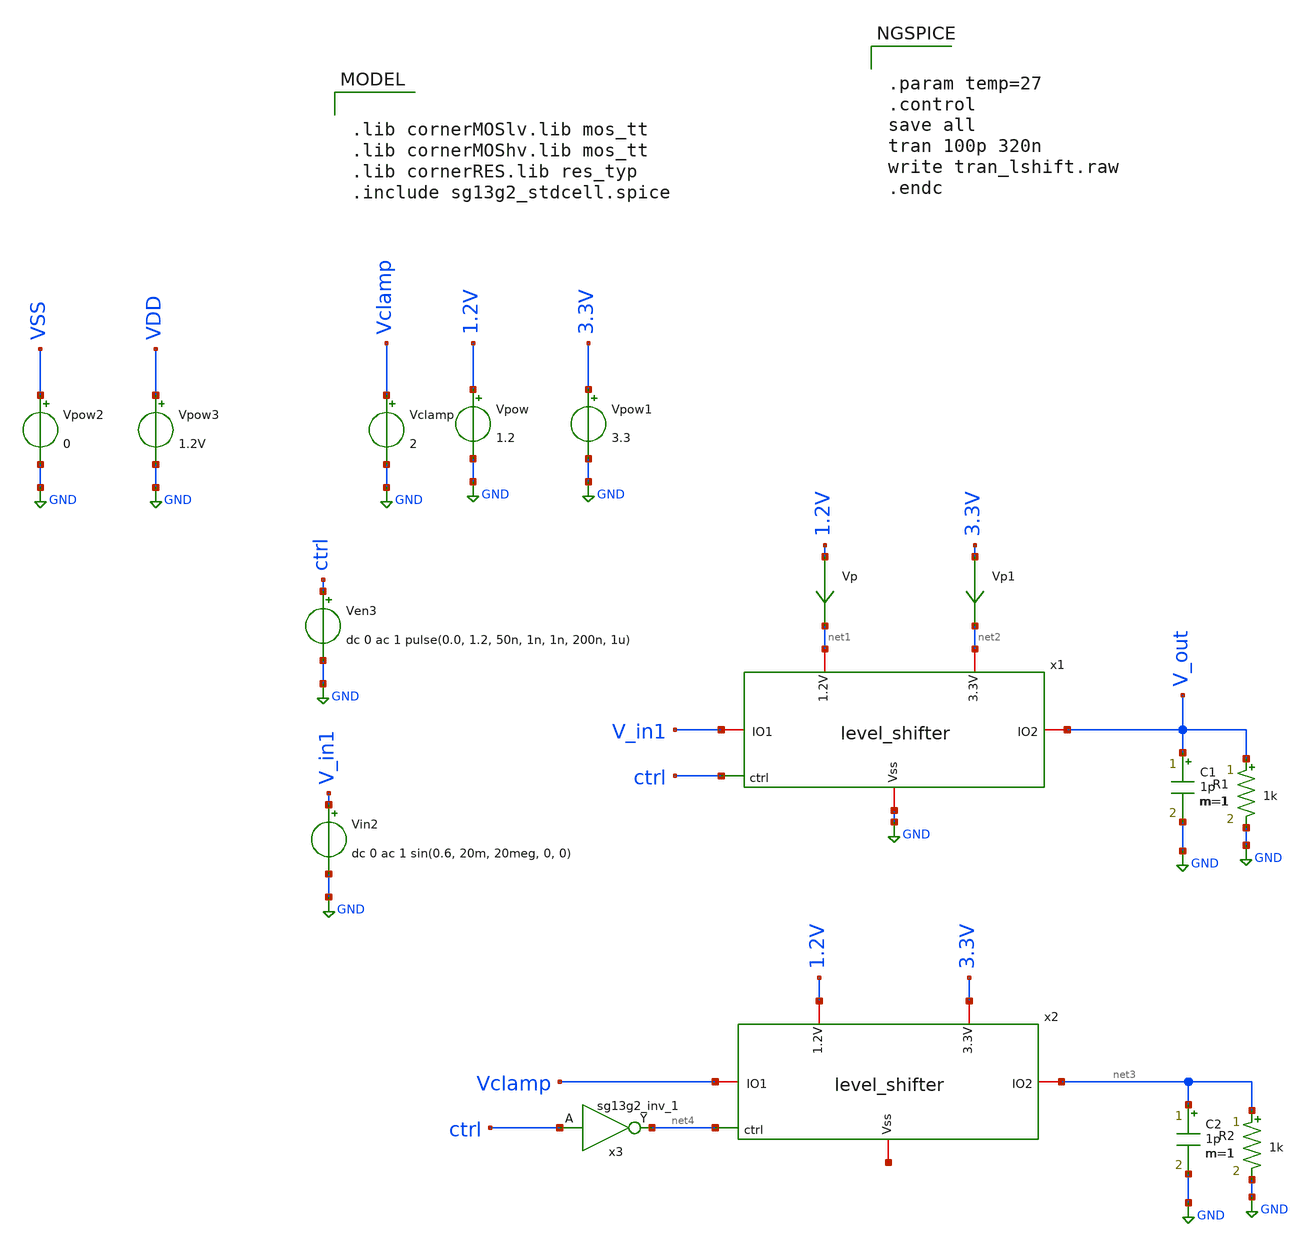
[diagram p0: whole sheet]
** sch_path: design_data/xschem/level_shifters_tb.sch
* Copyright 2023 IHP PDK Authors
* design_data/xschem/level_shifter.sch:
* Copyright 2025 IHP PDK Authors
**.subckt level_shifters_tb
Vpow 1.2V GND 1.2
Vp 1.2V net1 0
.save i(vp)
C1 V_out GND 1p m=1
Ven3 ctrl GND dc 0 ac 1 pulse(0.0, 1.2, 50n, 1n, 1n, 200n, 1u)
Vin2 V_in1 GND dc 0 ac 1 sin(0.6, 20m, 20meg, 0, 0)
Vpow1 3.3V GND 3.3
Vp1 3.3V net2 0
.save i(vp1)
x1 net1 V_out net2 ctrl V_in1 GND level_shifter
x2 1.2V net3 3.3V net4 Vclamp net5 level_shifter
x3 net4 ctrl VDD VSS sg13g2_inv_1
Vclamp Vclamp GND 2
Vpow2 VSS GND 0
Vpow3 VDD GND 1.2V
R1 V_out GND 1k m=1
C2 net3 GND 1p m=1
R2 net3 GND 1k m=1
**** begin user architecture code

.lib cornerMOSlv.lib mos_tt
.lib cornerMOShv.lib mos_tt
.lib cornerRES.lib res_typ
.include sg13g2_stdcell.spice



.param temp=27
.control
save all
tran 100p 320n
write tran_lshift.raw
.endc


**** end user architecture code
**.ends

* expanding   symbol:  level_shifter.sym # of pins=6
** sym_path: design_data/xschem/level_shifter.sym
** sch_path: design_data/xschem/level_shifter.sch
.subckt level_shifter 1.2V IO2 3.3V ctrl IO1 Vss
*.iopin IO1
*.iopin Vss
*.iopin IO2
*.iopin 3.3V
*.ipin ctrl
*.iopin 1.2V
XM2 net2 net1 3.3V 3.3V sg13_hv_pmos w=0.3u l=0.4u ng=1 m=1 mm_ok=1
XM3 net3 ctrl Vss Vss sg13_lv_nmos w=0.15u l=0.13u ng=1 m=1 mm_ok=1
XM5 net3 ctrl 1.2V net4 sg13_lv_pmos w=0.15u l=0.13u ng=1 m=1 mm_ok=1
XM6 net1 net3 Vss Vss sg13_lv_nmos w=0.15u l=0.13u ng=1 m=1 mm_ok=1
XM7 net2 ctrl Vss Vss sg13_lv_nmos w=0.15u l=0.13u ng=1 m=1 mm_ok=1
XM1 net1 net2 3.3V 3.3V sg13_hv_pmos w=0.3u l=0.4u ng=1 m=1 mm_ok=1
XM4 IO1 net1 IO2 3.3V sg13_hv_pmos w=0.3u l=0.4u ng=1 m=1 mm_ok=1
XM8 IO2 net2 IO1 Vss sg13_hv_nmos w=0.3u l=0.45u ng=1 m=1 mm_ok=1
.ends


* expanding   symbol:  sg13g2_stdcells/sg13g2_inv_1.sym # of pins=2
** sym_path: sg13g2_stdcells/sg13g2_inv_1.sym
** sch_path: sg13g2_stdcells/sg13g2_inv_1.sch
.subckt sg13g2_inv_1 Y A VDD VSS
*.opin Y
*.ipin A
*.iopin VDD
*.iopin VSS
XM1 Y A VSS VSS sg13_lv_nmos w=740.00n l=130.00n ng=1 m=1 mm_ok=1
XM2 Y A VDD VDD sg13_lv_pmos w=1.12u l=130.00n ng=1 m=1 mm_ok=1
.ends

.GLOBAL GND
.end
